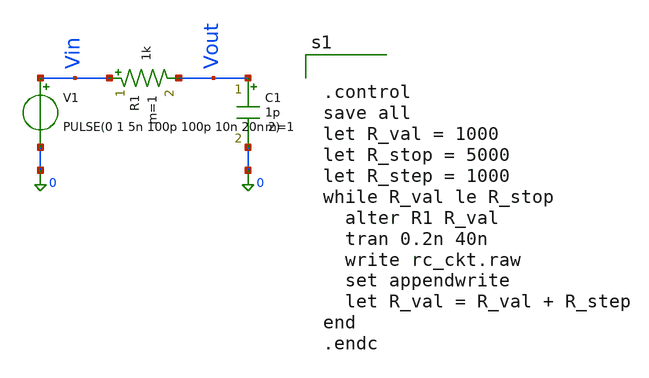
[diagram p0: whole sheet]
** sch_path: Lab_01/Lab_01.sch
**.subckt Lab_01
R1 Vin Vout 1k m=1
C1 Vout 0 1p m=1
V1 Vin 0 PULSE(0 1 5n 100p 100p 10n 20n 2)
**** begin user architecture code


.control
save all
let R_val = 1000
let R_stop = 5000
let R_step = 1000
while R_val le R_stop
  alter R1 R_val
  tran 0.2n 40n
  write rc_ckt.raw
  set appendwrite
  let R_val = R_val + R_step
end
.endc


**** end user architecture code
**.ends
.end
